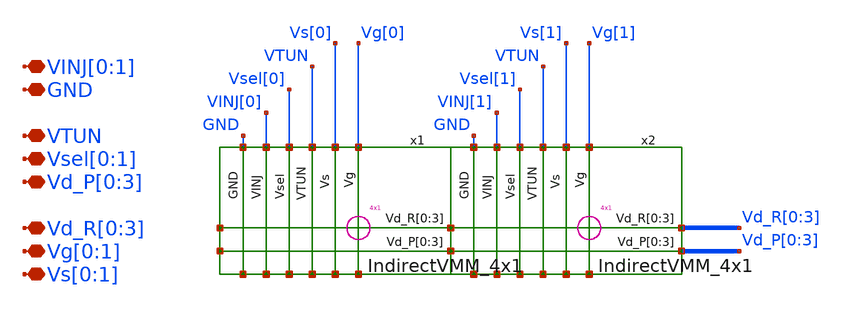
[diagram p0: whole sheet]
** sch_path: sky130_cells/IndirectVMM_4x2/IndirectVMM_4x2.sch
**.subckt IndirectVMM_4x2 Vd_R[0],Vd_R[1],Vd_R[2],Vd_R[3] Vd_P[0],Vd_P[1],Vd_P[2],Vd_P[3]
*+ Vg[0],Vg[1] VTUN Vsel[0],Vsel[1] GND VINJ[0],VINJ[1] Vs[0],Vs[1]
*.iopin Vd_R[0],Vd_R[1],Vd_R[2],Vd_R[3]
*.iopin Vd_P[0],Vd_P[1],Vd_P[2],Vd_P[3]
*.iopin Vg[0],Vg[1]
*.iopin VTUN
*.iopin Vsel[0],Vsel[1]
*.iopin GND
*.iopin VINJ[0],VINJ[1]
*.iopin Vs[0],Vs[1]
x1 Vd_P[0] Vd_P[1] Vd_P[2] Vd_P[3] Vd_R[0] Vd_R[1] Vd_R[2] Vd_R[3] Vg[0] Vs[0] VTUN Vsel[0] VINJ[0]
+ GND IndirectVMM_4x1
x2 Vd_P[0] Vd_P[1] Vd_P[2] Vd_P[3] Vd_R[0] Vd_R[1] Vd_R[2] Vd_R[3] Vg[1] Vs[1] VTUN Vsel[1] VINJ[1]
+ GND IndirectVMM_4x1
**.ends

* expanding   symbol:  sky130_cells/IndirectVMM_4x1/IndirectVMM_4x1.sym # of pins=16
** sym_path: sky130_cells/IndirectVMM_4x1/IndirectVMM_4x1.sym
** sch_path: sky130_cells/IndirectVMM_4x1/IndirectVMM_4x1.sch
.subckt IndirectVMM_4x1 Vd_P[0] Vd_P[1] Vd_P[2] Vd_P[3] Vd_R[0] Vd_R[1] Vd_R[2] Vd_R[3] Vg Vs VTUN
+ Vsel VINJ GND
*.iopin Vd_R[0],Vd_R[1],Vd_R[2],Vd_R[3]
*.iopin Vd_P[0],Vd_P[1],Vd_P[2],Vd_P[3]
*.iopin Vg
*.iopin VTUN
*.iopin Vsel
*.iopin GND
*.iopin VINJ
*.iopin Vs
x5[0] Vs Vg Vsel VTUN Vd_R[0] Vd_P[0] VINJ GND FG_Indirect
x5[1] Vs Vg Vsel VTUN Vd_R[1] Vd_P[1] VINJ GND FG_Indirect
x5[2] Vs Vg Vsel VTUN Vd_R[2] Vd_P[2] VINJ GND FG_Indirect
x5[3] Vs Vg Vsel VTUN Vd_R[3] Vd_P[3] VINJ GND FG_Indirect
.ends


* expanding   symbol:  sky130_cells/Floating_Gates/Indirect/FG_Indirect.sym # of pins=16
** sym_path: sky130_cells/Floating_Gates/Indirect/FG_Indirect.sym
** sch_path: sky130_cells/Floating_Gates/Indirect/FG_Indirect.sch
.subckt FG_Indirect Vs Vg Vsel VTUN Vd_R Vd_P VINJ GND
*.iopin VINJ
*.iopin Vsel
*.iopin Vg
*.iopin Vs
*.iopin Vd_R
*.iopin Vd_P
*.iopin VTUN
*.iopin GND
XM1 Vd_R Vfg Vs VINJ sky130_fd_pr__pfet_g5v0d10v5 L=0.5 W=0.42 nf=1 ad='int((nf+1)/2) * W/nf * 0.29'
+ as='int((nf+2)/2) * W/nf * 0.29' pd='2*int((nf+1)/2) * (W/nf + 0.29)' ps='2*int((nf+2)/2) * (W/nf + 0.29)'
+ nrd='0.29 / W' nrs='0.29 / W' sa=0 sb=0 sd=0 mult=1 m=1
XM2 net1 Vsel VINJ VINJ sky130_fd_pr__pfet_g5v0d10v5 L=0.5 W=0.42 nf=1 ad='int((nf+1)/2) * W/nf * 0.29'
+ as='int((nf+2)/2) * W/nf * 0.29' pd='2*int((nf+1)/2) * (W/nf + 0.29)' ps='2*int((nf+2)/2) * (W/nf + 0.29)'
+ nrd='0.29 / W' nrs='0.29 / W' sa=0 sb=0 sd=0 mult=1 m=1
XM3 Vd_P Vfg net1 VINJ sky130_fd_pr__pfet_g5v0d10v5 L=0.5 W=0.42 nf=1 ad='int((nf+1)/2) * W/nf * 0.29'
+ as='int((nf+2)/2) * W/nf * 0.29' pd='2*int((nf+1)/2) * (W/nf + 0.29)' ps='2*int((nf+2)/2) * (W/nf + 0.29)'
+ nrd='0.29 / W' nrs='0.29 / W' sa=0 sb=0 sd=0 mult=1 m=1
XC1 Vfg VTUN GND sky130_fd_pr__cap_var_hvt W=0.29 L=0.5 VM=1 m=1
XC2 Vfg Vg GND sky130_fd_pr__cap_var_hvt W=0.54 L=0.65 VM=1 m=1
.ends

.end
